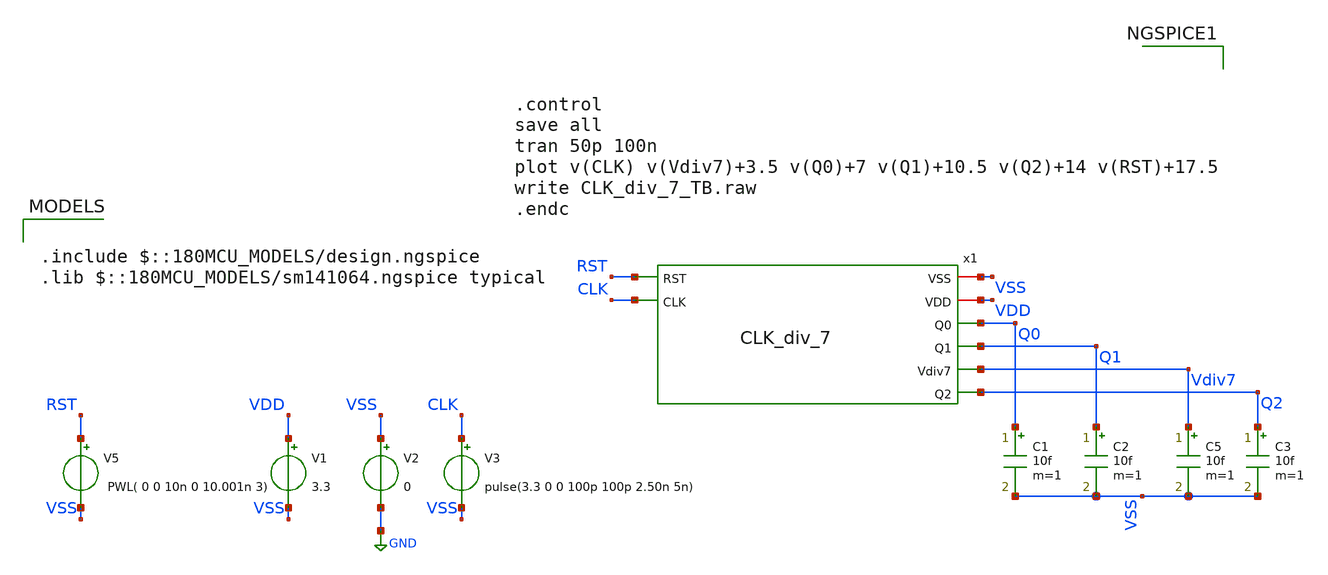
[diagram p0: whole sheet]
** sch_path: Clock_Generator_PAKISTAN_02/Schematics/CLK_div_7_TB_new.sch
**.subckt CLK_div_7_TB_new
V1 VDD VSS 3.3
V2 VSS GND 0
V3 CLK VSS pulse(3.3 0 0 100p 100p 2.50n 5n)
C1 Q0 VSS 10f m=1
C2 Q1 VSS 10f m=1
C5 Vdiv7 VSS 10f m=1
V5 RST VSS PWL( 0 0 10n 0 10.001n 3)
C3 Q2 VSS 10f m=1
x1 VSS VDD Q0 Q1 RST Vdiv7 Q2 CLK CLK_div_7
**** begin user architecture code

.include $::180MCU_MODELS/design.ngspice
.lib $::180MCU_MODELS/sm141064.ngspice typical




.control
save all
tran 50p 100n
plot v(CLK) v(Vdiv7)+3.5 v(Q0)+7 v(Q1)+10.5 v(Q2)+14 v(RST)+17.5
write CLK_div_7_TB.raw
.endc


**** end user architecture code
**.ends
.GLOBAL GND
.end
